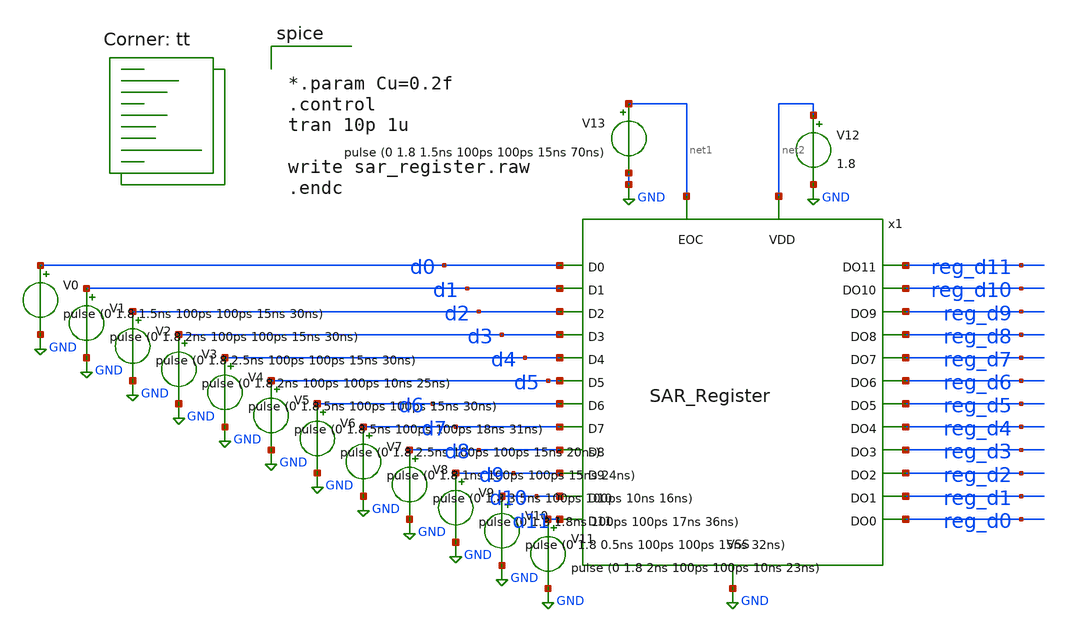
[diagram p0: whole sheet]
** sch_path: SAR_Register_tb.sch
**.subckt SAR_Register_tb
x1 net2 d8 d5 d11 d2 reg_d11 reg_d8 reg_d5 reg_d2 net1 d7 d1 d10 d4 reg_d1 reg_d4 reg_d7 reg_d10 d0
+ d3 d6 d9 reg_d0 reg_d3 reg_d6 reg_d9 GND SAR_Register
V1 d1 GND pulse (0 1.8 2ns 100ps 100ps 15ns 30ns)
V2 d2 GND pulse (0 1.8 2.5ns 100ps 100ps 15ns 30ns)
V3 d3 GND pulse (0 1.8 2ns 100ps 100ps 10ns 25ns)
V4 d4 GND pulse (0 1.8 5ns 100ps 100ps 15ns 30ns)
V5 d5 GND pulse (0 1.8 5ns 100ps 100ps 18ns 31ns)
V6 d6 GND pulse (0 1.8 2.5ns 100ps 100ps 15ns 20ns)
V7 d7 GND pulse (0 1.8 1ns 100ps 100ps 15ns 24ns)
V8 d8 GND pulse (0 1.8 3.5ns 100ps 100ps 10ns 16ns)
V9 d9 GND pulse (0 1.8 1.8ns 100ps 100ps 17ns 36ns)
V10 d10 GND pulse (0 1.8 0.5ns 100ps 100ps 15ns 32ns)
V11 d11 GND pulse (0 1.8 2ns 100ps 100ps 10ns 23ns)
V0 d0 GND pulse (0 1.8 1.5ns 100ps 100ps 15ns 30ns)
V12 net2 GND 1.8
V13 net1 GND pulse (0 1.8 1.5ns 100ps 100ps 15ns 70ns)
**** begin user architecture code
.lib $::SKYWATER_MODELS/sky130.lib.spice tt


*.param Cu=0.2f
.control
tran 10p 1u

write sar_register.raw
.endc


**** end user architecture code
**.ends

* expanding   symbol:  project/SAR_Register.sym # of pins=27
** sym_path: SAR_Register.sym
** sch_path: SAR_Register.sch
.subckt SAR_Register VDD D8 D5 D11 D2 DO11 DO8 DO5 DO2 EOC D7 D1 D10 D4 DO1 DO4 DO7 DO10 D0 D3 D6 D9
+ DO0 DO3 DO6 DO9 VSS
*.ipin VDD
*.ipin VSS
*.ipin D11
*.ipin D10
*.ipin D9
*.ipin D8
*.ipin D7
*.ipin D6
*.ipin D5
*.ipin D4
*.ipin D3
*.ipin D2
*.ipin D1
*.ipin D0
*.opin DO11
*.opin DO10
*.opin DO9
*.opin DO8
*.opin DO7
*.opin DO6
*.opin DO3
*.opin DO4
*.opin DO5
*.opin DO2
*.opin DO1
*.opin DO0
*.ipin EOC
x1 VDD EOC D11 DO11 VSS FFD_SVL
x2 VDD EOC D8 DO8 VSS FFD_SVL
x3 VDD EOC D5 DO5 VSS FFD_SVL
x4 VDD EOC D2 DO2 VSS FFD_SVL
x5 VDD EOC D10 DO10 VSS FFD_SVL
x6 VDD EOC D7 DO7 VSS FFD_SVL
x7 VDD EOC D4 DO4 VSS FFD_SVL
x8 VDD EOC D1 DO1 VSS FFD_SVL
x9 VDD EOC D9 DO9 VSS FFD_SVL
x10 VDD EOC D6 DO6 VSS FFD_SVL
x11 VDD EOC D3 DO3 VSS FFD_SVL
x12 VDD EOC D0 DO0 VSS FFD_SVL
.ends


* expanding   symbol:  project/FFD_SVL.sym # of pins=5
** sym_path: FFD_SVL.sym
** sch_path: FFD_SVL.sch
.subckt FFD_SVL VDD CLOCK IN OUT VSS
*.ipin VDD
*.ipin VSS
*.opin OUT
*.ipin IN
*.ipin CLOCK
XM1 net1 CLKB VDD VDD sky130_fd_pr__pfet_01v8 L=0.15 W=1 nf=1 ad='int((nf+1)/2) * W/nf * 0.29' as='int((nf+2)/2) * W/nf * 0.29'
+ pd='2*int((nf+1)/2) * (W/nf + 0.29)' ps='2*int((nf+2)/2) * (W/nf + 0.29)' nrd='0.29 / W' nrs='0.29 / W'
+ sa=0 sb=0 sd=0 mult=1 m=1
XM2 VDD VDD net1 VDD sky130_fd_pr__nfet_01v8 L=0.15 W=1 nf=1 ad='int((nf+1)/2) * W/nf * 0.29' as='int((nf+2)/2) * W/nf * 0.29'
+ pd='2*int((nf+1)/2) * (W/nf + 0.29)' ps='2*int((nf+2)/2) * (W/nf + 0.29)' nrd='0.29 / W' nrs='0.29 / W'
+ sa=0 sb=0 sd=0 mult=1 m=1
XM3 VSS VSS net4 VDD sky130_fd_pr__pfet_01v8 L=0.15 W=1 nf=1 ad='int((nf+1)/2) * W/nf * 0.29' as='int((nf+2)/2) * W/nf * 0.29'
+ pd='2*int((nf+1)/2) * (W/nf + 0.29)' ps='2*int((nf+2)/2) * (W/nf + 0.29)' nrd='0.29 / W' nrs='0.29 / W'
+ sa=0 sb=0 sd=0 mult=1 m=1
XM4 net4 CLK VSS VSS sky130_fd_pr__nfet_01v8 L=0.15 W=1 nf=1 ad='int((nf+1)/2) * W/nf * 0.29' as='int((nf+2)/2) * W/nf * 0.29'
+ pd='2*int((nf+1)/2) * (W/nf + 0.29)' ps='2*int((nf+2)/2) * (W/nf + 0.29)' nrd='0.29 / W' nrs='0.29 / W'
+ sa=0 sb=0 sd=0 mult=1 m=1
XM5 net2 IN net1 VDD sky130_fd_pr__pfet_01v8 L=0.15 W=1 nf=1 ad='int((nf+1)/2) * W/nf * 0.29' as='int((nf+2)/2) * W/nf * 0.29'
+ pd='2*int((nf+1)/2) * (W/nf + 0.29)' ps='2*int((nf+2)/2) * (W/nf + 0.29)' nrd='0.29 / W' nrs='0.29 / W'
+ sa=0 sb=0 sd=0 mult=1 m=1
XM6 OUT net2 net1 VDD sky130_fd_pr__pfet_01v8 L=0.15 W=1 nf=1 ad='int((nf+1)/2) * W/nf * 0.29' as='int((nf+2)/2) * W/nf * 0.29'
+ pd='2*int((nf+1)/2) * (W/nf + 0.29)' ps='2*int((nf+2)/2) * (W/nf + 0.29)' nrd='0.29 / W' nrs='0.29 / W'
+ sa=0 sb=0 sd=0 mult=1 m=1
XM7 net2 CLK net3 VSS sky130_fd_pr__nfet_01v8 L=0.15 W=1 nf=1 ad='int((nf+1)/2) * W/nf * 0.29' as='int((nf+2)/2) * W/nf * 0.29'
+ pd='2*int((nf+1)/2) * (W/nf + 0.29)' ps='2*int((nf+2)/2) * (W/nf + 0.29)' nrd='0.29 / W' nrs='0.29 / W'
+ sa=0 sb=0 sd=0 mult=1 m=1
XM8 net3 IN net4 VSS sky130_fd_pr__nfet_01v8 L=0.15 W=1 nf=1 ad='int((nf+1)/2) * W/nf * 0.29' as='int((nf+2)/2) * W/nf * 0.29'
+ pd='2*int((nf+1)/2) * (W/nf + 0.29)' ps='2*int((nf+2)/2) * (W/nf + 0.29)' nrd='0.29 / W' nrs='0.29 / W'
+ sa=0 sb=0 sd=0 mult=1 m=1
XM9 OUT net3 net4 VSS sky130_fd_pr__nfet_01v8 L=0.15 W=1 nf=1 ad='int((nf+1)/2) * W/nf * 0.29' as='int((nf+2)/2) * W/nf * 0.29'
+ pd='2*int((nf+1)/2) * (W/nf + 0.29)' ps='2*int((nf+2)/2) * (W/nf + 0.29)' nrd='0.29 / W' nrs='0.29 / W'
+ sa=0 sb=0 sd=0 mult=1 m=1
x7 VDD CLOCK CLKB VSS Inverter
x8 VDD CLKB CLK VSS Inverter
.ends


* expanding   symbol:  project/Inverter.sym # of pins=4
** sym_path: Inverter.sym
** sch_path: Inverter.sch
.subckt Inverter VDD IN OUT VSS
*.ipin IN
*.ipin VSS
*.ipin VDD
*.opin OUT
XM1 OUT IN VSS VSS sky130_fd_pr__nfet_01v8 L=0.3 W=1 nf=1 ad='int((nf+1)/2) * W/nf * 0.29' as='int((nf+2)/2) * W/nf * 0.29'
+ pd='2*int((nf+1)/2) * (W/nf + 0.29)' ps='2*int((nf+2)/2) * (W/nf + 0.29)' nrd='0.29 / W' nrs='0.29 / W'
+ sa=0 sb=0 sd=0 mult=1 m=1
XM2 OUT IN VDD VDD sky130_fd_pr__pfet_01v8 L=0.3 W=2 nf=1 ad='int((nf+1)/2) * W/nf * 0.29' as='int((nf+2)/2) * W/nf * 0.29'
+ pd='2*int((nf+1)/2) * (W/nf + 0.29)' ps='2*int((nf+2)/2) * (W/nf + 0.29)' nrd='0.29 / W' nrs='0.29 / W'
+ sa=0 sb=0 sd=0 mult=1 m=1
.ends

.GLOBAL GND
.end
